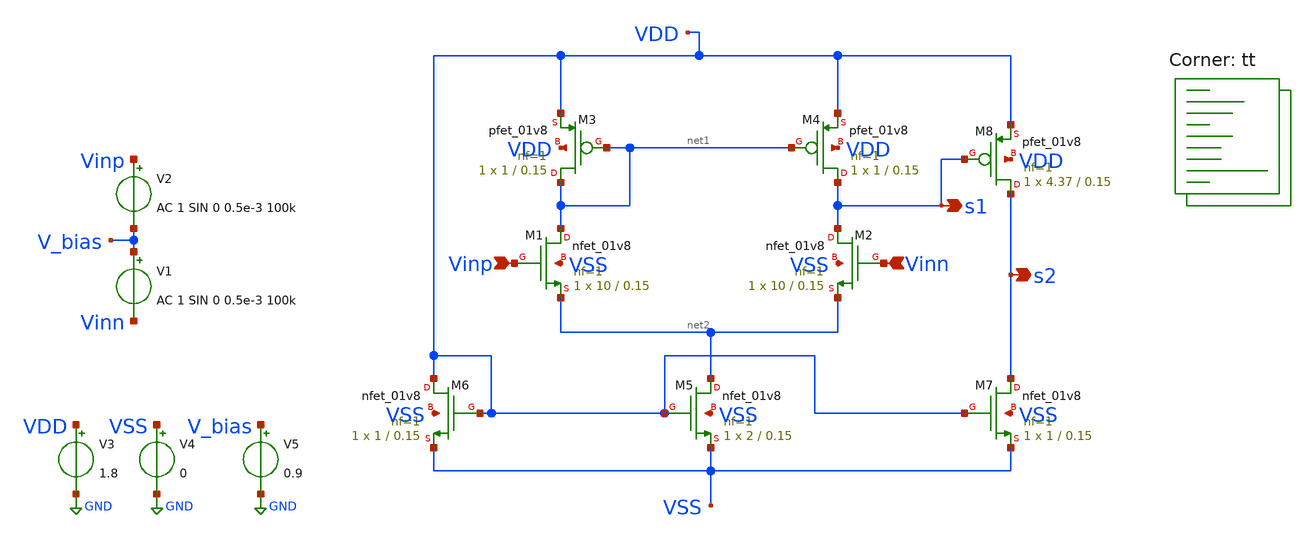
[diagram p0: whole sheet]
** sch_path: xschem/src/opamp_hw02.sch
**.subckt opamp_hw02 Vinp Vinn s2 s1
*.ipin Vinp
*.ipin Vinn
*.opin s2
*.opin s1
XM1 net1 Vinp net2 VSS sky130_fd_pr__nfet_01v8 L=0.15 W=10 nf=1 ad='int((nf+1)/2) * W/nf * 0.29' as='int((nf+2)/2) * W/nf * 0.29'
+ pd='2*int((nf+1)/2) * (W/nf + 0.29)' ps='2*int((nf+2)/2) * (W/nf + 0.29)' nrd='0.29 / W' nrs='0.29 / W'
+ sa=0 sb=0 sd=0 mult=1 m=1
XM2 s1 Vinn net2 VSS sky130_fd_pr__nfet_01v8 L=0.15 W=10 nf=1 ad='int((nf+1)/2) * W/nf * 0.29' as='int((nf+2)/2) * W/nf * 0.29'
+ pd='2*int((nf+1)/2) * (W/nf + 0.29)' ps='2*int((nf+2)/2) * (W/nf + 0.29)' nrd='0.29 / W' nrs='0.29 / W'
+ sa=0 sb=0 sd=0 mult=1 m=1
XM3 net1 net1 VDD VDD sky130_fd_pr__pfet_01v8 L=0.15 W=1 nf=1 ad='int((nf+1)/2) * W/nf * 0.29' as='int((nf+2)/2) * W/nf * 0.29'
+ pd='2*int((nf+1)/2) * (W/nf + 0.29)' ps='2*int((nf+2)/2) * (W/nf + 0.29)' nrd='0.29 / W' nrs='0.29 / W'
+ sa=0 sb=0 sd=0 mult=1 m=1
XM4 s1 net1 VDD VDD sky130_fd_pr__pfet_01v8 L=0.15 W=1 nf=1 ad='int((nf+1)/2) * W/nf * 0.29' as='int((nf+2)/2) * W/nf * 0.29'
+ pd='2*int((nf+1)/2) * (W/nf + 0.29)' ps='2*int((nf+2)/2) * (W/nf + 0.29)' nrd='0.29 / W' nrs='0.29 / W'
+ sa=0 sb=0 sd=0 mult=1 m=1
XM5 net2 VDD VSS VSS sky130_fd_pr__nfet_01v8 L=0.15 W=2 nf=1 ad='int((nf+1)/2) * W/nf * 0.29' as='int((nf+2)/2) * W/nf * 0.29'
+ pd='2*int((nf+1)/2) * (W/nf + 0.29)' ps='2*int((nf+2)/2) * (W/nf + 0.29)' nrd='0.29 / W' nrs='0.29 / W'
+ sa=0 sb=0 sd=0 mult=1 m=1
XM6 VDD VDD VSS VSS sky130_fd_pr__nfet_01v8 L=0.15 W=1 nf=1 ad='int((nf+1)/2) * W/nf * 0.29' as='int((nf+2)/2) * W/nf * 0.29'
+ pd='2*int((nf+1)/2) * (W/nf + 0.29)' ps='2*int((nf+2)/2) * (W/nf + 0.29)' nrd='0.29 / W' nrs='0.29 / W'
+ sa=0 sb=0 sd=0 mult=1 m=1
XM7 s2 VDD VSS VSS sky130_fd_pr__nfet_01v8 L=0.15 W=1 nf=1 ad='int((nf+1)/2) * W/nf * 0.29' as='int((nf+2)/2) * W/nf * 0.29'
+ pd='2*int((nf+1)/2) * (W/nf + 0.29)' ps='2*int((nf+2)/2) * (W/nf + 0.29)' nrd='0.29 / W' nrs='0.29 / W'
+ sa=0 sb=0 sd=0 mult=1 m=1
XM8 s2 s1 VDD VDD sky130_fd_pr__pfet_01v8 L=0.15 W=4.37 nf=1 ad='int((nf+1)/2) * W/nf * 0.29' as='int((nf+2)/2) * W/nf * 0.29'
+ pd='2*int((nf+1)/2) * (W/nf + 0.29)' ps='2*int((nf+2)/2) * (W/nf + 0.29)' nrd='0.29 / W' nrs='0.29 / W'
+ sa=0 sb=0 sd=0 mult=1 m=1
V1 V_bias Vinn AC 1 SIN 0 0.5e-3 100k
V2 Vinp V_bias AC 1 SIN 0 0.5e-3 100k
V3 VDD GND 1.8
V4 VSS GND 0
V5 V_bias GND 0.9
**** begin user architecture code
.lib $::SKYWATER_MODELS/sky130.lib.spice tt



* ngspice commands
.options method=gear

.control
save all
ac dec 10 1 3.2e9
plot dB(s1)
plot dB(s2)
tran 1n 50u
plot s2
plot v3#branch
.endc



**** end user architecture code
**.ends
.GLOBAL GND
.end
